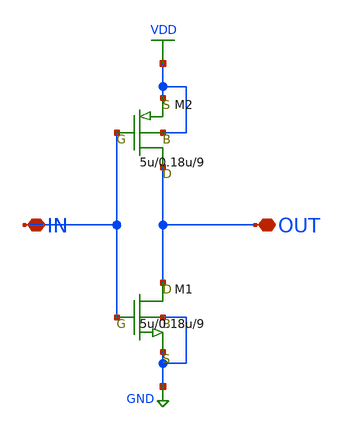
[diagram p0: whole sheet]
** sch_path: LR_hasegawa/LR_Work2/Citizen035/INVERTER9_Citizen.sch
**.subckt INVERTER9_Citizen OUT IN
*.iopin OUT
*.iopin IN
M1 OUT IN GND GND nch w=5u l=0.18u as=0 ps=0 ad=0 pd=0 m=9
M2 OUT IN VDD VDD pch w=5u l=0.18u as=0 ps=0 ad=0 pd=0 m=9
**.ends
.GLOBAL VDD
.GLOBAL GND
.end
